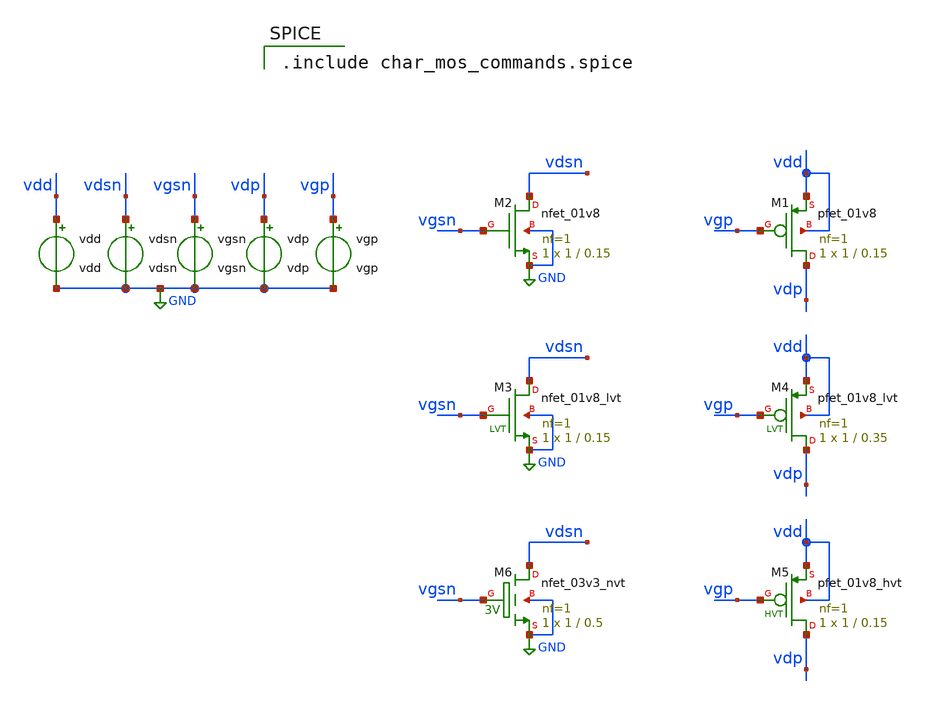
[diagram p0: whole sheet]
** sch_path: designs/char_mos.sch
**.subckt char_mos
vdsn vdsn GND vdsn
vgsn vgsn GND vgsn
XM2 vdsn vgsn GND GND sky130_fd_pr__nfet_01v8 L=0.15 W=1 nf=1 ad='int((nf+1)/2) * W/nf * 0.29' as='int((nf+2)/2) * W/nf * 0.29'
+ pd='2*int((nf+1)/2) * (W/nf + 0.29)' ps='2*int((nf+2)/2) * (W/nf + 0.29)' nrd='0.29 / W' nrs='0.29 / W'
+ sa=0 sb=0 sd=0 mult=1 m=1
vdd vdd GND vdd
vdp vdp GND vdp
vgp vgp GND vgp
XM1 vdp vgp vdd vdd sky130_fd_pr__pfet_01v8 L=0.15 W=1 nf=1 ad='int((nf+1)/2) * W/nf * 0.29' as='int((nf+2)/2) * W/nf * 0.29'
+ pd='2*int((nf+1)/2) * (W/nf + 0.29)' ps='2*int((nf+2)/2) * (W/nf + 0.29)' nrd='0.29 / W' nrs='0.29 / W'
+ sa=0 sb=0 sd=0 mult=1 m=1
XM4 vdp vgp vdd vdd sky130_fd_pr__pfet_01v8_lvt L=0.35 W=1 nf=1 ad='int((nf+1)/2) * W/nf * 0.29' as='int((nf+2)/2) * W/nf * 0.29'
+ pd='2*int((nf+1)/2) * (W/nf + 0.29)' ps='2*int((nf+2)/2) * (W/nf + 0.29)' nrd='0.29 / W' nrs='0.29 / W'
+ sa=0 sb=0 sd=0 mult=1 m=1
XM3 vdsn vgsn GND GND sky130_fd_pr__nfet_01v8_lvt L=0.15 W=1 nf=1 ad='int((nf+1)/2) * W/nf * 0.29' as='int((nf+2)/2) * W/nf * 0.29'
+ pd='2*int((nf+1)/2) * (W/nf + 0.29)' ps='2*int((nf+2)/2) * (W/nf + 0.29)' nrd='0.29 / W' nrs='0.29 / W'
+ sa=0 sb=0 sd=0 mult=1 m=1
XM5 vdp vgp vdd vdd sky130_fd_pr__pfet_01v8_hvt L=0.15 W=1 nf=1 ad='int((nf+1)/2) * W/nf * 0.29' as='int((nf+2)/2) * W/nf * 0.29'
+ pd='2*int((nf+1)/2) * (W/nf + 0.29)' ps='2*int((nf+2)/2) * (W/nf + 0.29)' nrd='0.29 / W' nrs='0.29 / W'
+ sa=0 sb=0 sd=0 mult=1 m=1
XM6 vdsn vgsn GND GND sky130_fd_pr__nfet_03v3_nvt L=0.5 W=1 nf=1 ad='int((nf+1)/2) * W/nf * 0.29' as='int((nf+2)/2) * W/nf * 0.29'
+ pd='2*int((nf+1)/2) * (W/nf + 0.29)' ps='2*int((nf+2)/2) * (W/nf + 0.29)' nrd='0.29 / W' nrs='0.29 / W'
+ sa=0 sb=0 sd=0 mult=1 m=1
**** begin user architecture code

.include char_mos_commands.spice

**** end user architecture code
**.ends
.GLOBAL GND
.end
